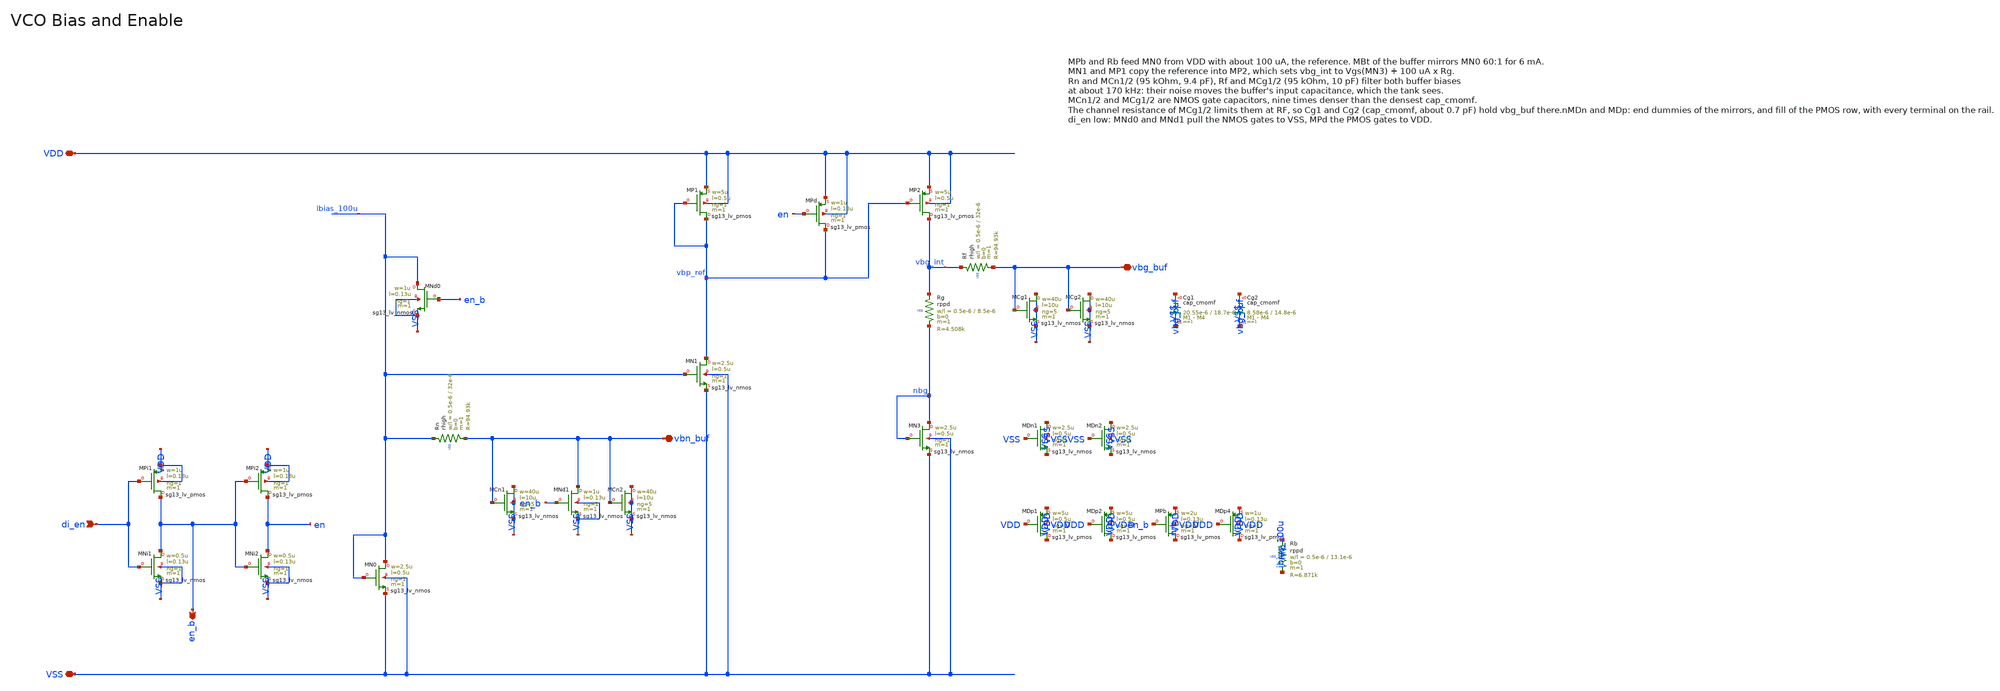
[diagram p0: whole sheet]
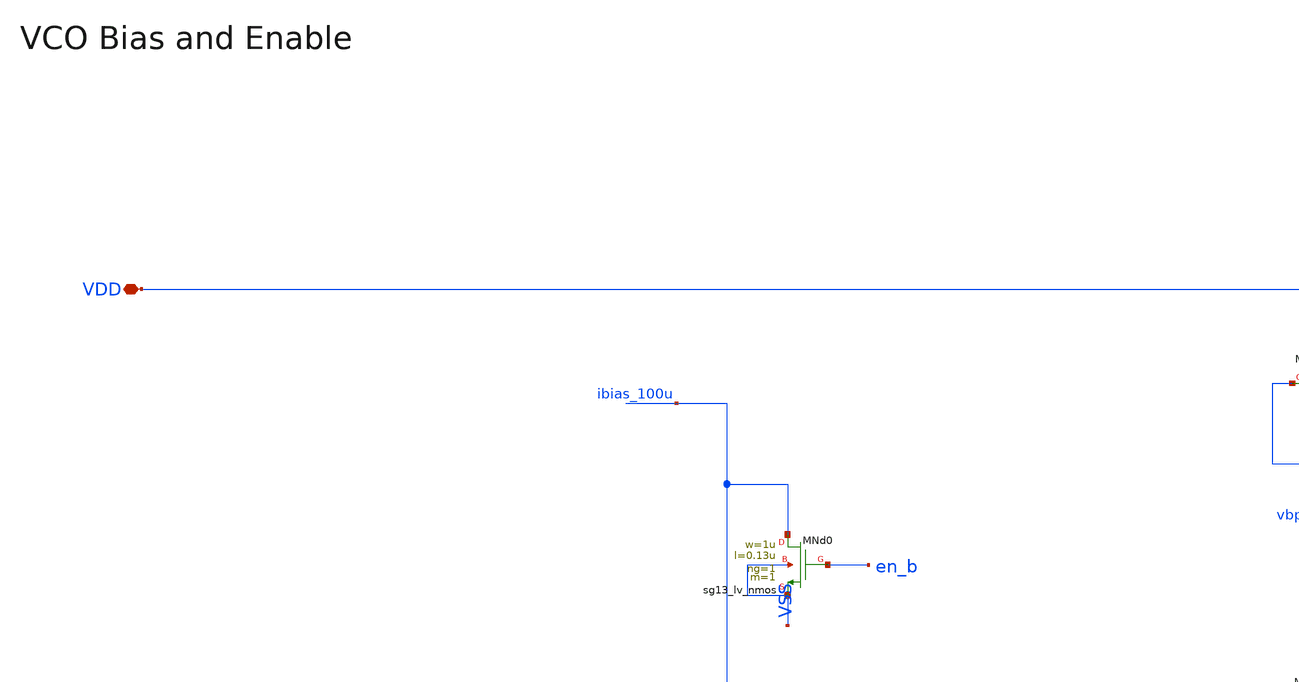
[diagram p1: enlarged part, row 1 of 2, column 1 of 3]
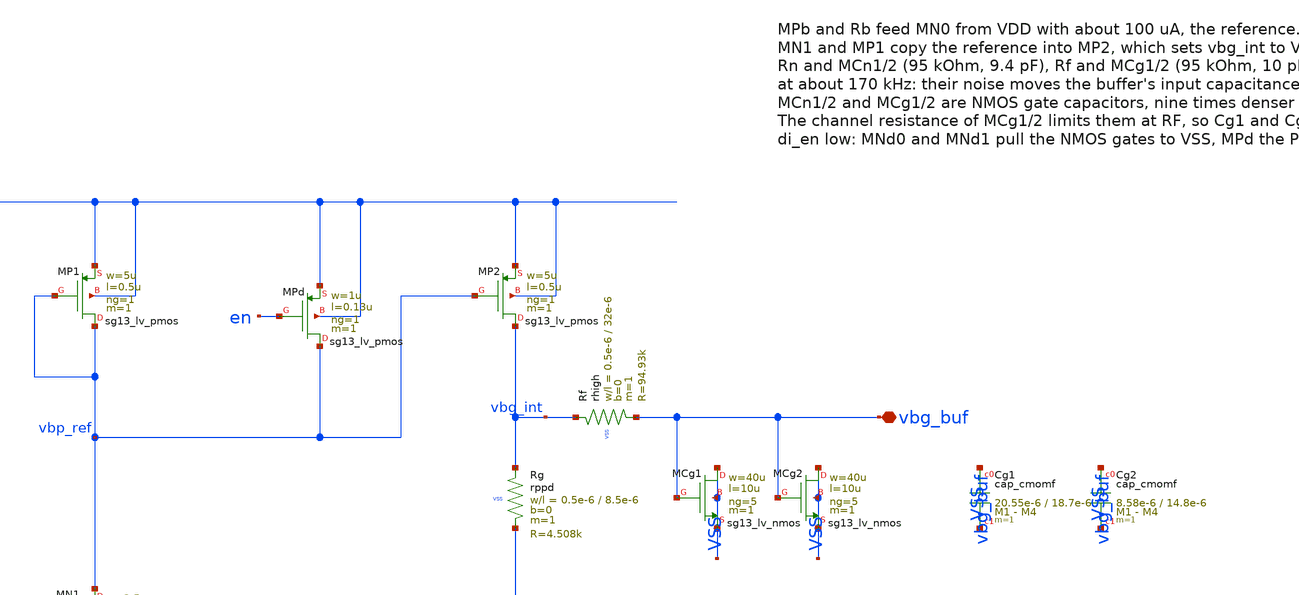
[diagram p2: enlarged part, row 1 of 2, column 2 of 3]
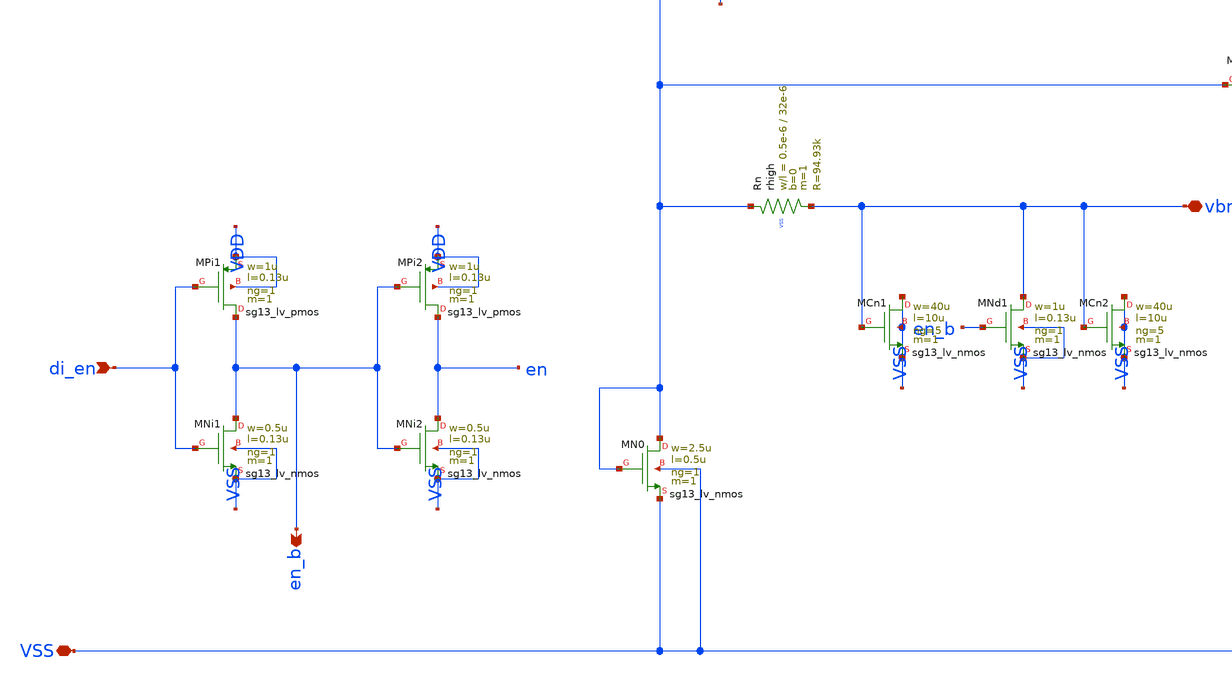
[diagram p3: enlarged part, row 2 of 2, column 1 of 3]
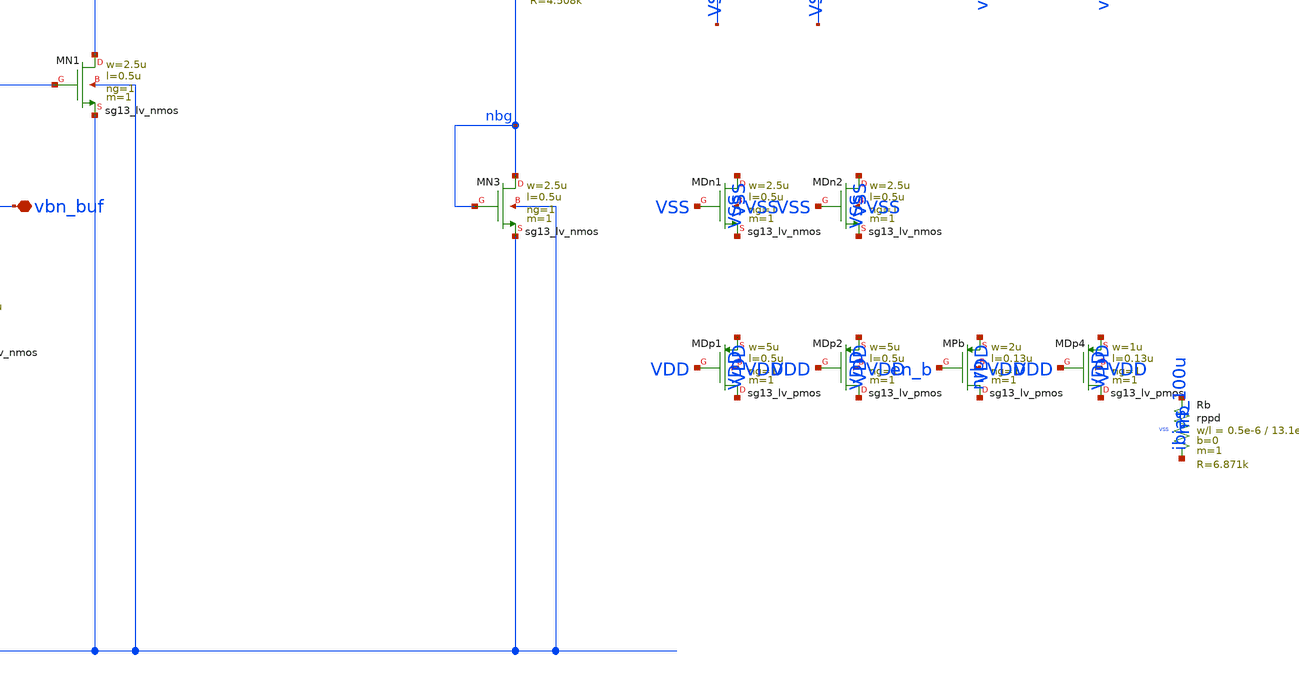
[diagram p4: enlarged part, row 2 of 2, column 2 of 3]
** sch_path: macros/vco/schematic/xschem/vco_bias.sch
**.subckt vco_bias VDD VSS di_en en_b vbn_buf vbg_buf
*.iopin VDD
*.iopin VSS
*.ipin di_en
*.opin en_b
*.iopin vbn_buf
*.iopin vbg_buf
XMPi1 en_b di_en VDD VDD sg13_lv_pmos w=1u l=0.13u ng=1 m=1 mm_ok=1
XMNi1 en_b di_en VSS VSS sg13_lv_nmos w=0.5u l=0.13u ng=1 m=1 mm_ok=1
XMPi2 en en_b VDD VDD sg13_lv_pmos w=1u l=0.13u ng=1 m=1 mm_ok=1
XMNi2 en en_b VSS VSS sg13_lv_nmos w=0.5u l=0.13u ng=1 m=1 mm_ok=1
XMN0 ibias_100u ibias_100u VSS VSS sg13_lv_nmos w=2.5u l=0.5u ng=1 m=1 mm_ok=1
XMNd0 ibias_100u en_b VSS VSS sg13_lv_nmos w=1u l=0.13u ng=1 m=1 mm_ok=1
XRn ibias_100u vbn_buf VSS rhigh w=0.5e-6 l=32e-6 m=1 b=0 mm_ok=1
XMNd1 vbn_buf en_b VSS VSS sg13_lv_nmos w=1u l=0.13u ng=1 m=1 mm_ok=1
XMN1 vbp_ref ibias_100u VSS VSS sg13_lv_nmos w=2.5u l=0.5u ng=1 m=1 mm_ok=1
XMP1 vbp_ref vbp_ref VDD VDD sg13_lv_pmos w=5u l=0.5u ng=1 m=1 mm_ok=1
XMPd vbp_ref en VDD VDD sg13_lv_pmos w=1u l=0.13u ng=1 m=1 mm_ok=1
XMP2 vbg_int vbp_ref VDD VDD sg13_lv_pmos w=5u l=0.5u ng=1 m=1 mm_ok=1
XRg vbg_int nbg VSS rppd w=0.5e-6 l=8.5e-6 m=1 b=0 mm_ok=1
XMN3 nbg nbg VSS VSS sg13_lv_nmos w=2.5u l=0.5u ng=1 m=1 mm_ok=1
XMCn1 VSS vbn_buf VSS VSS sg13_lv_nmos w=40u l=10u ng=5 m=1 mm_ok=1
XMCn2 VSS vbn_buf VSS VSS sg13_lv_nmos w=40u l=10u ng=5 m=1 mm_ok=1
XRf vbg_int vbg_buf VSS rhigh w=0.5e-6 l=32e-6 m=1 b=0 mm_ok=1
XMCg1 VSS vbg_buf VSS VSS sg13_lv_nmos w=40u l=10u ng=5 m=1 mm_ok=1
XMCg2 VSS vbg_buf VSS VSS sg13_lv_nmos w=40u l=10u ng=5 m=1 mm_ok=1
XMDn1 VSS VSS VSS VSS sg13_lv_nmos w=2.5u l=0.5u ng=1 m=1 mm_ok=1
XMDn2 VSS VSS VSS VSS sg13_lv_nmos w=2.5u l=0.5u ng=1 m=1 mm_ok=1
XMDp1 VDD VDD VDD VDD sg13_lv_pmos w=5u l=0.5u ng=1 m=1 mm_ok=1
XMDp2 VDD VDD VDD VDD sg13_lv_pmos w=5u l=0.5u ng=1 m=1 mm_ok=1
XMPb nrb en_b VDD VDD sg13_lv_pmos w=2u l=0.13u ng=1 m=1 mm_ok=1
XMDp4 VDD VDD VDD VDD sg13_lv_pmos w=1u l=0.13u ng=1 m=1 mm_ok=1
XRb nrb ibias_100u VSS rppd w=0.5e-6 l=13.1e-6 m=1 b=0 mm_ok=1
XCg1 vbg_buf VSS cap_cmomf w=20.55e-6 l=18.7e-6 mmin=1 mmax=4 subblock=0 rfmodel=0 subscale=1 m=1
+ mm_ok=1
XCg2 vbg_buf VSS cap_cmomf w=8.58e-6 l=14.8e-6 mmin=1 mmax=4 subblock=0 rfmodel=0 subscale=1 m=1
+ mm_ok=1
**.ends
.end
